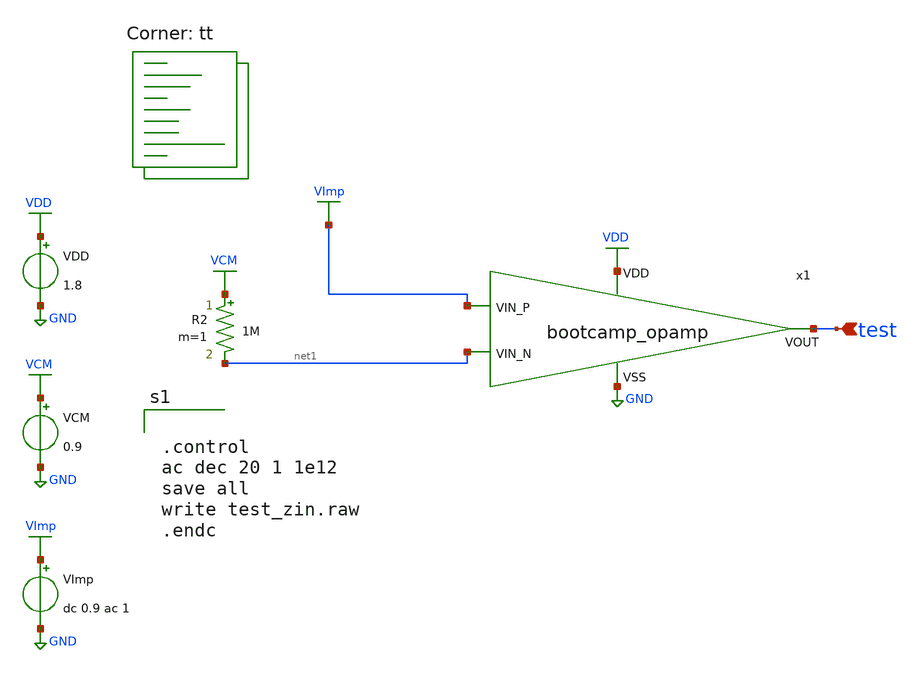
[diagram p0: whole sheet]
** sch_path: analog/schematics/tb_impedance.sch
**.subckt tb_impedance test
*.ipin test
x1 VDD test net1 VImp GND bootcamp_opamp
R2 VCM net1 1M m=1
VDD VDD GND 1.8
VCM VCM GND 0.9
VImp VImp GND dc 0.9 ac 1
**** begin user architecture code


.control
ac dec 20 1 1e12
save all
write test_zin.raw
.endc


.lib $::SKYWATER_MODELS/sky130.lib.spice tt
**** end user architecture code
**.ends

* expanding   symbol:  bootcamp_opamp.sym # of pins=5
** sym_path: analog/schematics/bootcamp_opamp.sym
** sch_path: analog/schematics/bootcamp_opamp.sch
.subckt bootcamp_opamp VDD VOUT VIN_N VIN_P VSS
*.ipin VIN_P
*.ipin VIN_N
*.ipin VDD
*.ipin VSS
*.opin VOUT
XM1 net1 VIN_P net3 VSS sky130_fd_pr__nfet_01v8 L=0.5 W=16 nf=1 ad='int((nf+1)/2) * W/nf * 0.29' as='int((nf+2)/2) * W/nf * 0.29'
+ pd='2*int((nf+1)/2) * (W/nf + 0.29)' ps='2*int((nf+2)/2) * (W/nf + 0.29)' nrd='0.29 / W' nrs='0.29 / W'
+ sa=0 sb=0 sd=0 mult=1 m=1
XM2 net2 VIN_N net3 VSS sky130_fd_pr__nfet_01v8 L=0.5 W=16 nf=1 ad='int((nf+1)/2) * W/nf * 0.29' as='int((nf+2)/2) * W/nf * 0.29'
+ pd='2*int((nf+1)/2) * (W/nf + 0.29)' ps='2*int((nf+2)/2) * (W/nf + 0.29)' nrd='0.29 / W' nrs='0.29 / W'
+ sa=0 sb=0 sd=0 mult=1 m=1
XM3 net1 net1 VDD VDD sky130_fd_pr__pfet_01v8 L=0.5 W=10 nf=1 ad='int((nf+1)/2) * W/nf * 0.29' as='int((nf+2)/2) * W/nf * 0.29'
+ pd='2*int((nf+1)/2) * (W/nf + 0.29)' ps='2*int((nf+2)/2) * (W/nf + 0.29)' nrd='0.29 / W' nrs='0.29 / W'
+ sa=0 sb=0 sd=0 mult=1 m=1
XM4 net2 net1 VDD VDD sky130_fd_pr__pfet_01v8 L=0.5 W=10 nf=1 ad='int((nf+1)/2) * W/nf * 0.29' as='int((nf+2)/2) * W/nf * 0.29'
+ pd='2*int((nf+1)/2) * (W/nf + 0.29)' ps='2*int((nf+2)/2) * (W/nf + 0.29)' nrd='0.29 / W' nrs='0.29 / W'
+ sa=0 sb=0 sd=0 mult=1 m=1
XM5 net3 VDD VSS VSS sky130_fd_pr__nfet_01v8 L=2 W=4 nf=1 ad='int((nf+1)/2) * W/nf * 0.29' as='int((nf+2)/2) * W/nf * 0.29'
+ pd='2*int((nf+1)/2) * (W/nf + 0.29)' ps='2*int((nf+2)/2) * (W/nf + 0.29)' nrd='0.29 / W' nrs='0.29 / W'
+ sa=0 sb=0 sd=0 mult=1 m=1
XM6 VOUT net2 VDD VDD sky130_fd_pr__pfet_01v8 L=0.5 W=10 nf=1 ad='int((nf+1)/2) * W/nf * 0.29' as='int((nf+2)/2) * W/nf * 0.29'
+ pd='2*int((nf+1)/2) * (W/nf + 0.29)' ps='2*int((nf+2)/2) * (W/nf + 0.29)' nrd='0.29 / W' nrs='0.29 / W'
+ sa=0 sb=0 sd=0 mult=1 m=1
XM7 VOUT VDD VSS VSS sky130_fd_pr__nfet_01v8 L=2 W=4 nf=1 ad='int((nf+1)/2) * W/nf * 0.29' as='int((nf+2)/2) * W/nf * 0.29'
+ pd='2*int((nf+1)/2) * (W/nf + 0.29)' ps='2*int((nf+2)/2) * (W/nf + 0.29)' nrd='0.29 / W' nrs='0.29 / W'
+ sa=0 sb=0 sd=0 mult=1 m=1
XM8 VDD VDD VSS VSS sky130_fd_pr__nfet_01v8 L=0.8 W=4 nf=1 ad='int((nf+1)/2) * W/nf * 0.29' as='int((nf+2)/2) * W/nf * 0.29'
+ pd='2*int((nf+1)/2) * (W/nf + 0.29)' ps='2*int((nf+2)/2) * (W/nf + 0.29)' nrd='0.29 / W' nrs='0.29 / W'
+ sa=0 sb=0 sd=0 mult=1 m=1
XC1 net2 VOUT sky130_fd_pr__cap_mim_m3_1 W=50 L=10 MF=1 m=1
.ends

.GLOBAL GND
.GLOBAL VDD
.GLOBAL VCM
.GLOBAL VImp
.end
